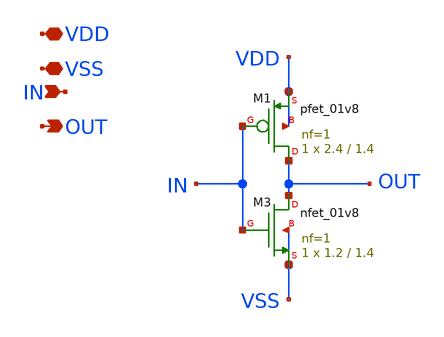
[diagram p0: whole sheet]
** sch_path: Xschem/PLL_TOP_Schematics/INV_NOCG.sch
**.subckt INV_NOCG VDD VSS IN OUT
*.iopin VDD
*.iopin VSS
*.ipin IN
*.opin OUT
XM1 OUT IN VDD VDD sky130_fd_pr__pfet_01v8 L=1.4 W=2.4 nf=1 ad='int((nf+1)/2) * W/nf * 0.29' as='int((nf+2)/2) * W/nf * 0.29'
+ pd='2*int((nf+1)/2) * (W/nf + 0.29)' ps='2*int((nf+2)/2) * (W/nf + 0.29)' nrd='0.29 / W' nrs='0.29 / W'
+ sa=0 sb=0 sd=0 mult=1 m=1
XM3 OUT IN VSS VSS sky130_fd_pr__nfet_01v8 L=1.4 W=1.2 nf=1 ad='int((nf+1)/2) * W/nf * 0.29' as='int((nf+2)/2) * W/nf * 0.29'
+ pd='2*int((nf+1)/2) * (W/nf + 0.29)' ps='2*int((nf+2)/2) * (W/nf + 0.29)' nrd='0.29 / W' nrs='0.29 / W'
+ sa=0 sb=0 sd=0 mult=1 m=1
**.ends
.end
